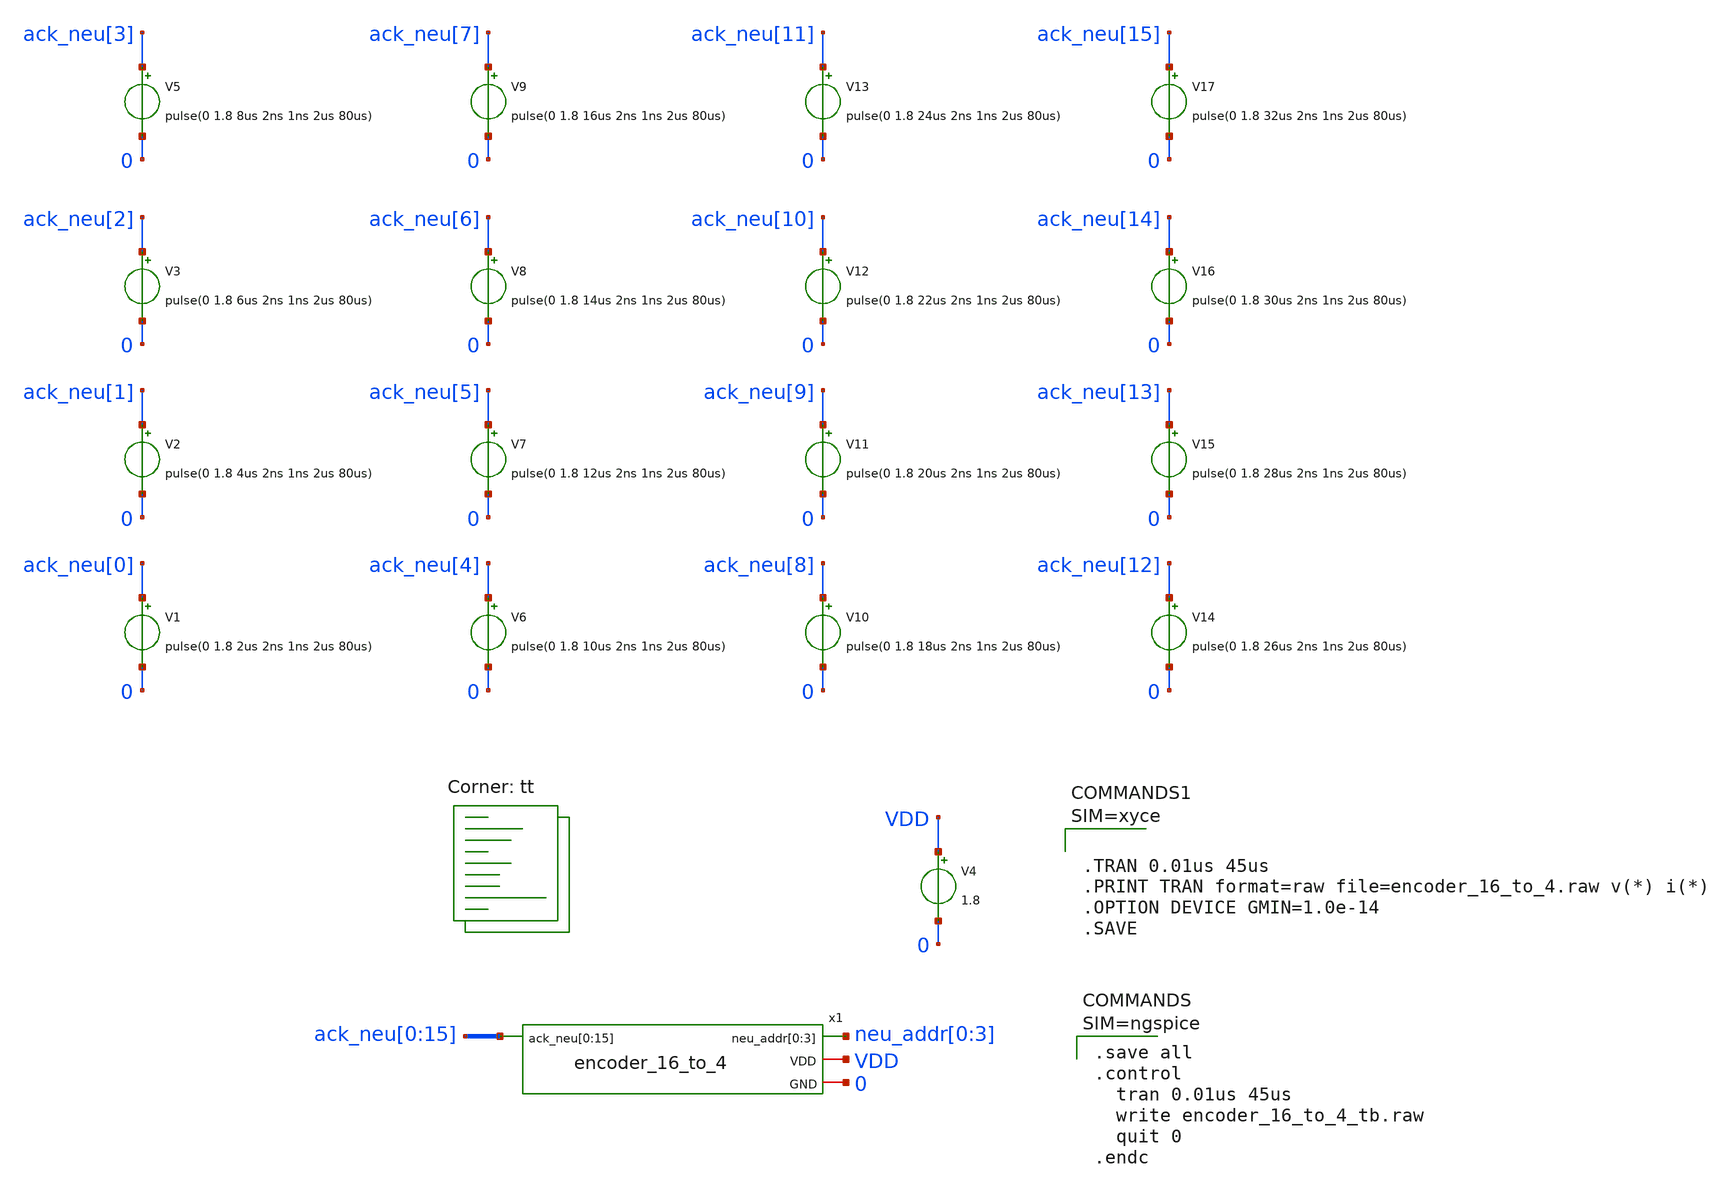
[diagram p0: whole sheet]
** sch_path: design/xschem/encoder_16_to_4_tb.sch
**.subckt encoder_16_to_4_tb
x1 neu_addr[0] neu_addr[1] neu_addr[2] neu_addr[3] ack_neu[0] ack_neu[1] ack_neu[2] ack_neu[3]
+ ack_neu[4] ack_neu[5] ack_neu[6] ack_neu[7] ack_neu[8] ack_neu[9] ack_neu[10] ack_neu[11] ack_neu[12]
+ ack_neu[13] ack_neu[14] ack_neu[15] VDD 0 encoder_16_to_4
V1 ack_neu[0] 0 pulse(0 1.8 2us 2ns 1ns 2us 80us)
V4 VDD 0 1.8
V2 ack_neu[1] 0 pulse(0 1.8 4us 2ns 1ns 2us 80us)
V3 ack_neu[2] 0 pulse(0 1.8 6us 2ns 1ns 2us 80us)
V5 ack_neu[3] 0 pulse(0 1.8 8us 2ns 1ns 2us 80us)
V6 ack_neu[4] 0 pulse(0 1.8 10us 2ns 1ns 2us 80us)
V7 ack_neu[5] 0 pulse(0 1.8 12us 2ns 1ns 2us 80us)
V8 ack_neu[6] 0 pulse(0 1.8 14us 2ns 1ns 2us 80us)
V9 ack_neu[7] 0 pulse(0 1.8 16us 2ns 1ns 2us 80us)
V10 ack_neu[8] 0 pulse(0 1.8 18us 2ns 1ns 2us 80us)
V11 ack_neu[9] 0 pulse(0 1.8 20us 2ns 1ns 2us 80us)
V12 ack_neu[10] 0 pulse(0 1.8 22us 2ns 1ns 2us 80us)
V13 ack_neu[11] 0 pulse(0 1.8 24us 2ns 1ns 2us 80us)
V14 ack_neu[12] 0 pulse(0 1.8 26us 2ns 1ns 2us 80us)
V15 ack_neu[13] 0 pulse(0 1.8 28us 2ns 1ns 2us 80us)
V16 ack_neu[14] 0 pulse(0 1.8 30us 2ns 1ns 2us 80us)
V17 ack_neu[15] 0 pulse(0 1.8 32us 2ns 1ns 2us 80us)
**** begin user architecture code


* Standard cell simulation files
.include $::SKYWATER_STDCELLS/sky130_fd_sc_hd.spice


.lib $::SKYWATER_MODELS/sky130.lib.spice tt


.save all
.control
  tran 0.01us 45us
  write encoder_16_to_4_tb.raw
  quit 0
.endc






**** end user architecture code
**.ends

* expanding   symbol:  encoder_16_to_4.sym # of pins=4
** sym_path: design/xschem/encoder_16_to_4.sym
** sch_path: design/xschem/encoder_16_to_4.sch
.subckt encoder_16_to_4 neu_addr[0] neu_addr[1] neu_addr[2] neu_addr[3] ack_neu[0] ack_neu[1]
+ ack_neu[2] ack_neu[3] ack_neu[4] ack_neu[5] ack_neu[6] ack_neu[7] ack_neu[8] ack_neu[9] ack_neu[10]
+ ack_neu[11] ack_neu[12] ack_neu[13] ack_neu[14] ack_neu[15] VDD GND
*.opin neu_addr[0],neu_addr[1],neu_addr[2],neu_addr[3]
*.ipin
*+ ack_neu[0],ack_neu[1],ack_neu[2],ack_neu[3],ack_neu[4],ack_neu[5],ack_neu[6],ack_neu[7],ack_neu[8],ack_neu[9],ack_neu[10],ack_neu[11],ack_neu[12],ack_neu[13],ack_neu[14],ack_neu[15]
*.iopin VDD
*.iopin GND
x1 ack_neu[8] ack_neu[9] ack_neu[10] ack_neu[11] neu_addr[3] ack_neu[12] ack_neu[13] ack_neu[14]
+ ack_neu[15] VDD GND or8
x2 ack_neu[4] ack_neu[5] ack_neu[6] ack_neu[7] neu_addr[2] ack_neu[12] ack_neu[13] ack_neu[14]
+ ack_neu[15] VDD GND or8
x3 ack_neu[2] ack_neu[3] ack_neu[6] ack_neu[7] neu_addr[1] ack_neu[10] ack_neu[11] ack_neu[14]
+ ack_neu[15] VDD GND or8
x4 ack_neu[1] ack_neu[3] ack_neu[5] ack_neu[7] neu_addr[0] ack_neu[9] ack_neu[11] ack_neu[13]
+ ack_neu[15] VDD GND or8
.ends


* expanding   symbol:  or8.sym # of pins=11
** sym_path: design/xschem/or8.sym
** sch_path: design/xschem/or8.sch
.subckt or8 h g f e out d c b a VDD GND
*.ipin a
*.ipin b
*.ipin c
*.ipin d
*.ipin e
*.ipin f
*.ipin g
*.ipin h
*.opin out
*.iopin VDD
*.iopin GND
x1 h g f e GND GND VDD VDD net1 sky130_fd_sc_hd__or4_1
x2 d c b a GND GND VDD VDD net2 sky130_fd_sc_hd__or4_1
x3 net1 net2 GND GND VDD VDD out sky130_fd_sc_hd__or2_1
.ends

.end
